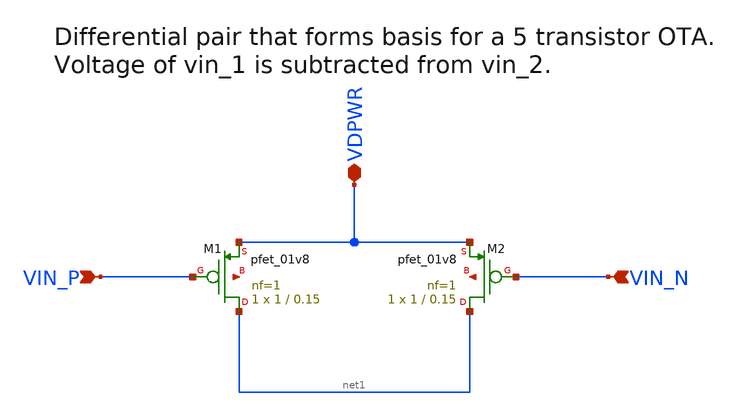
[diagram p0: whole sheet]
** sch_path: xschem/pfet_diff_pair.sch
**.subckt pfet_diff_pair VIN_P VIN_N VDPWR
*.ipin VIN_P
*.ipin VIN_N
*.iopin VDPWR
XM1 net1 VIN_P VDPWR net2 sky130_fd_pr__pfet_01v8 L=0.15 W=1 nf=1 ad='int((1 + 1)/2) * 1 / 1 * 0.29'
+ as='int((1 + 2)/2) * 1 / 1 * 0.29' pd='2*int((1 + 1)/2) * (1 / 1 + 0.29)' ps='2*int((1 + 2)/2) * (1 / 1 + 0.29)'
+ nrd='0.29 / 1 ' nrs='0.29 / 1 ' sa=0 sb=0 sd=0 mult=1 m=1
XM2 net1 VIN_N VDPWR net3 sky130_fd_pr__pfet_01v8 L=0.15 W=1 nf=1 ad='int((1 + 1)/2) * 1 / 1 * 0.29'
+ as='int((1 + 2)/2) * 1 / 1 * 0.29' pd='2*int((1 + 1)/2) * (1 / 1 + 0.29)' ps='2*int((1 + 2)/2) * (1 / 1 + 0.29)'
+ nrd='0.29 / 1 ' nrs='0.29 / 1 ' sa=0 sb=0 sd=0 mult=1 m=1
**.ends
.end
